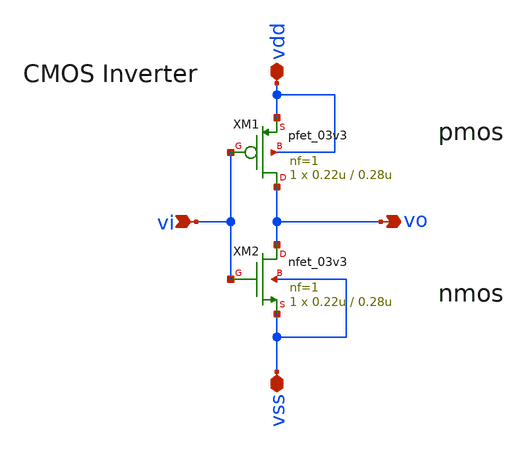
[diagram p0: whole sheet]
** sch_path: comparator/schematic/inv1.sch
**.subckt inv1 vi vo vdd vss
*.ipin vi
*.opin vo
*.iopin vdd
*.iopin vss
XM1 vo vi vdd vdd pfet_03v3 L=0.28u W=0.22u nf=1 ad='int((nf+1)/2) * W/nf * 0.18u' as='int((nf+2)/2) * W/nf * 0.18u'
+ pd='2*int((nf+1)/2) * (W/nf + 0.18u)' ps='2*int((nf+2)/2) * (W/nf + 0.18u)' nrd='0.18u / W' nrs='0.18u / W'
+ sa=0 sb=0 sd=0 m=1
XM2 vo vi vss vss nfet_03v3 L=0.28u W=0.22u nf=1 ad='int((nf+1)/2) * W/nf * 0.18u' as='int((nf+2)/2) * W/nf * 0.18u'
+ pd='2*int((nf+1)/2) * (W/nf + 0.18u)' ps='2*int((nf+2)/2) * (W/nf + 0.18u)' nrd='0.18u / W' nrs='0.18u / W'
+ sa=0 sb=0 sd=0 m=1
**.ends
.end
